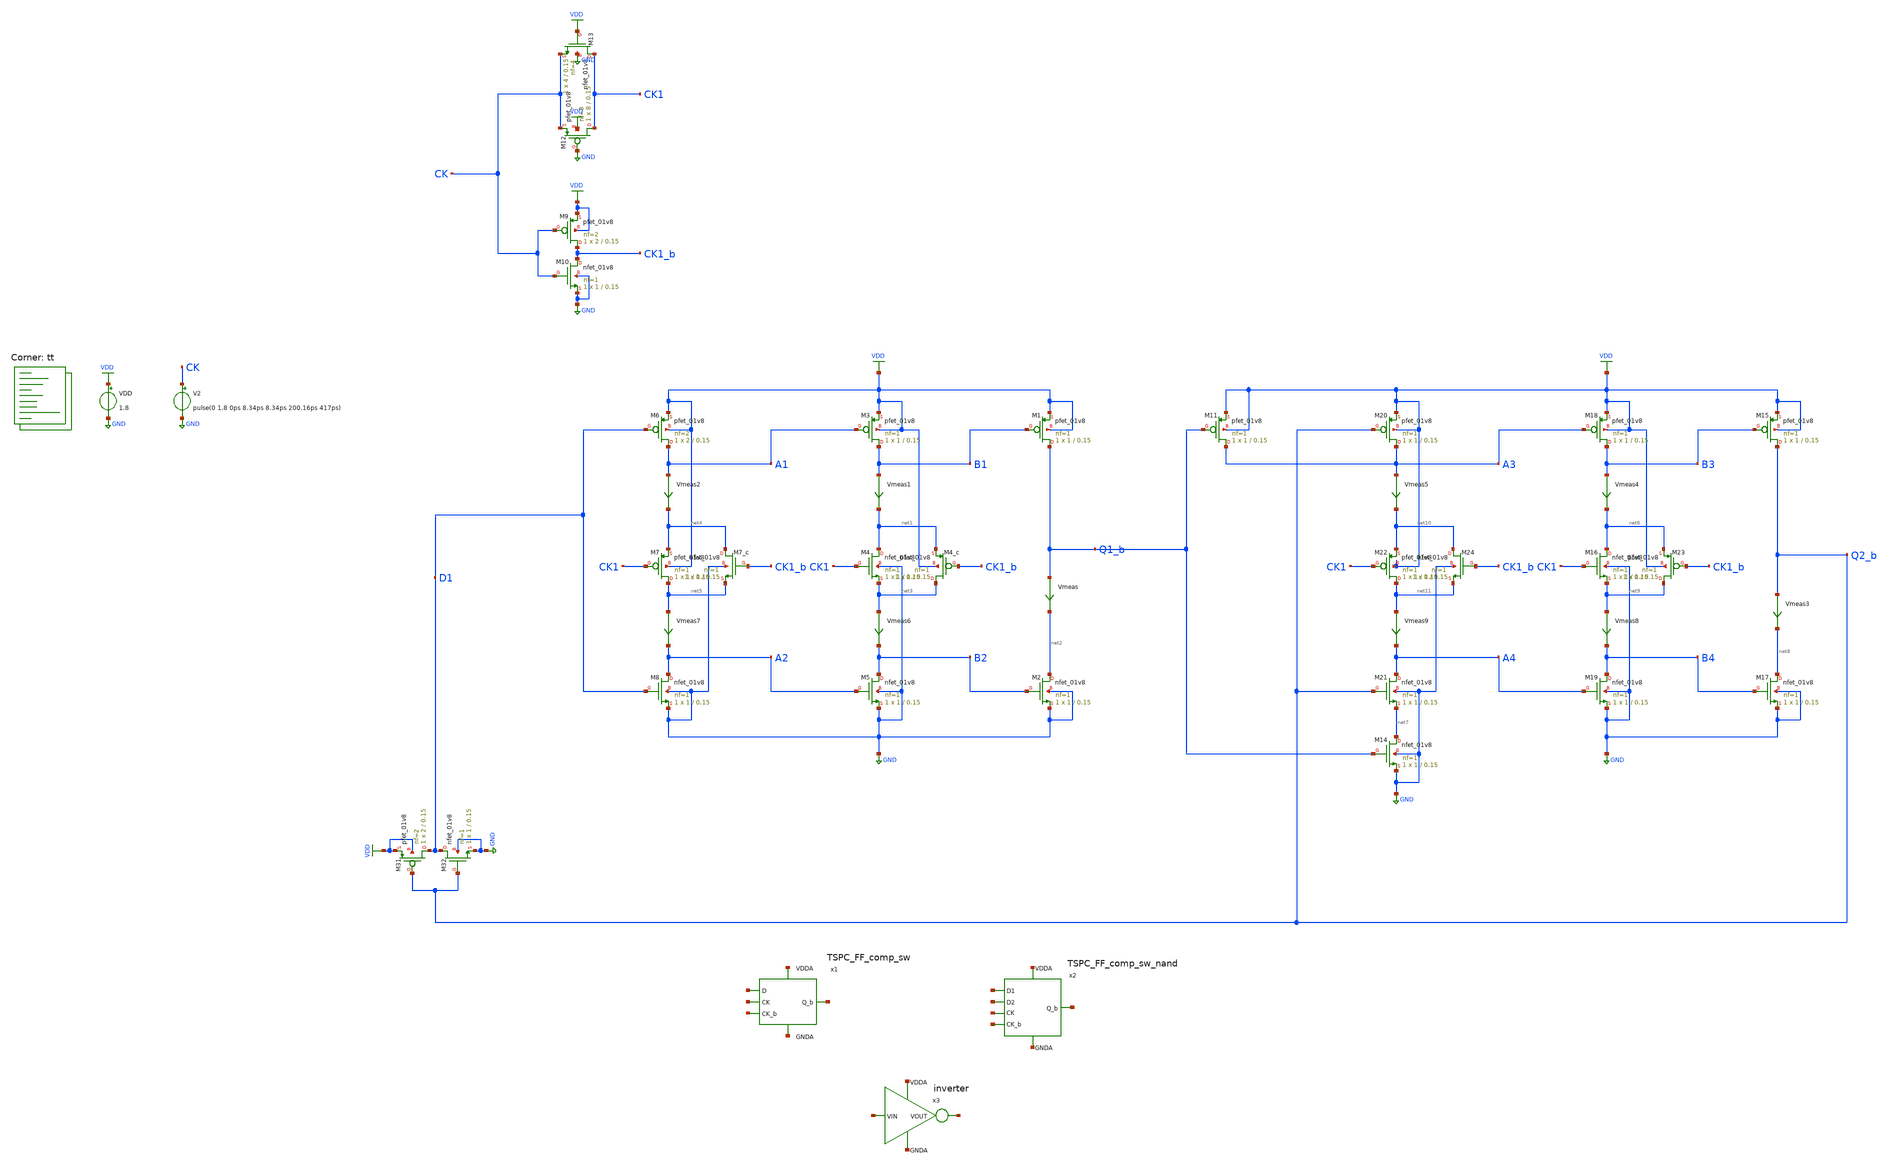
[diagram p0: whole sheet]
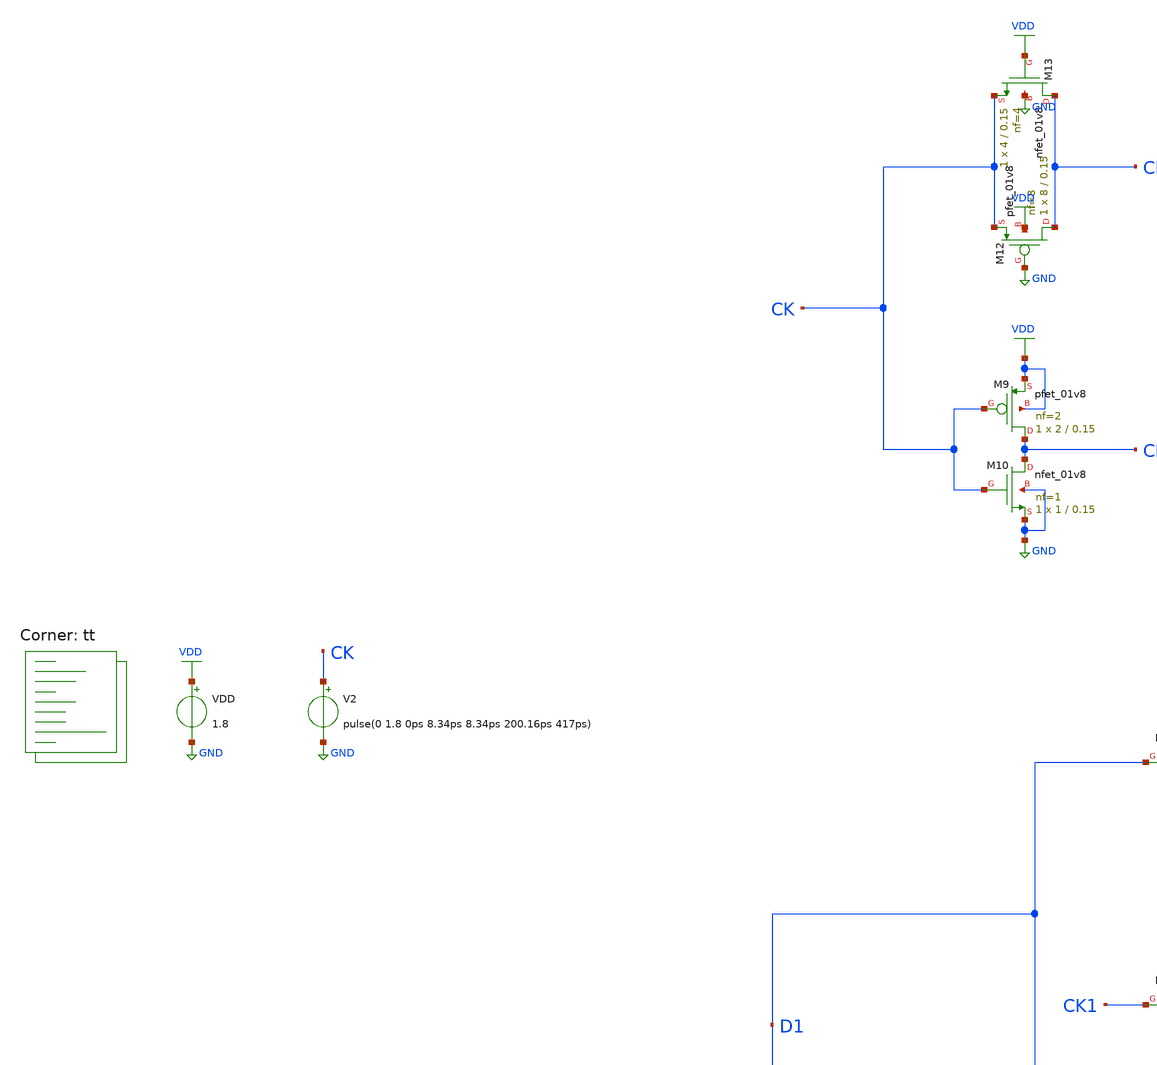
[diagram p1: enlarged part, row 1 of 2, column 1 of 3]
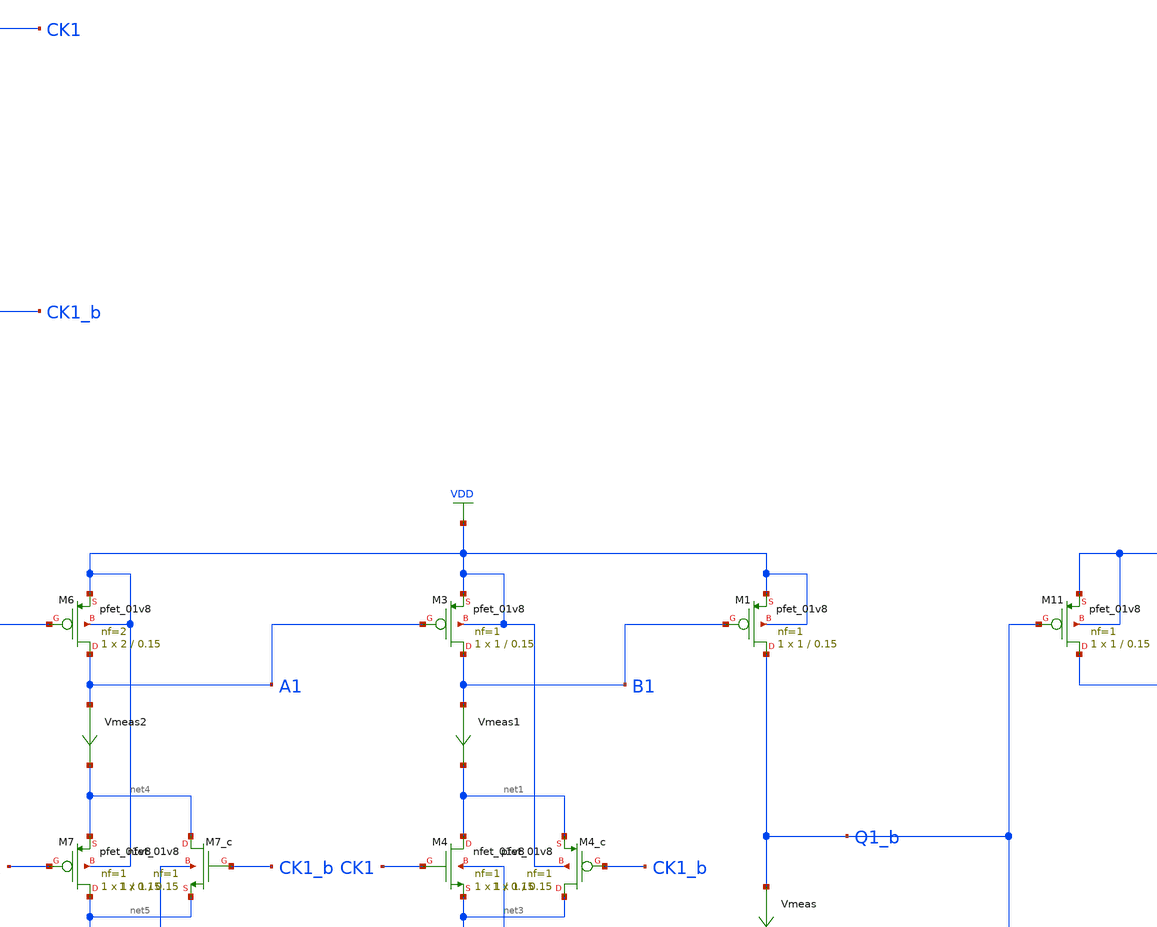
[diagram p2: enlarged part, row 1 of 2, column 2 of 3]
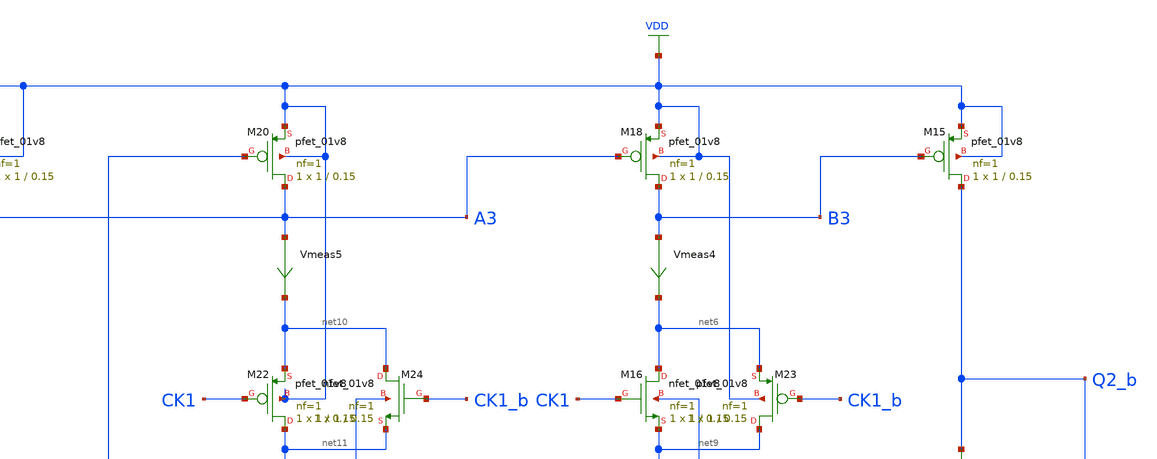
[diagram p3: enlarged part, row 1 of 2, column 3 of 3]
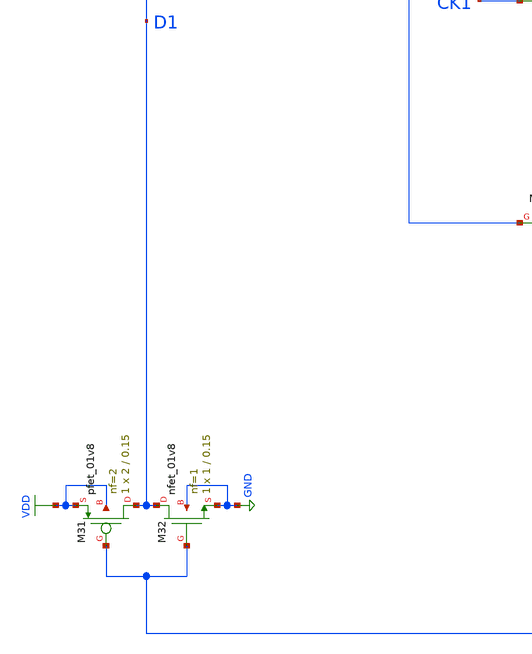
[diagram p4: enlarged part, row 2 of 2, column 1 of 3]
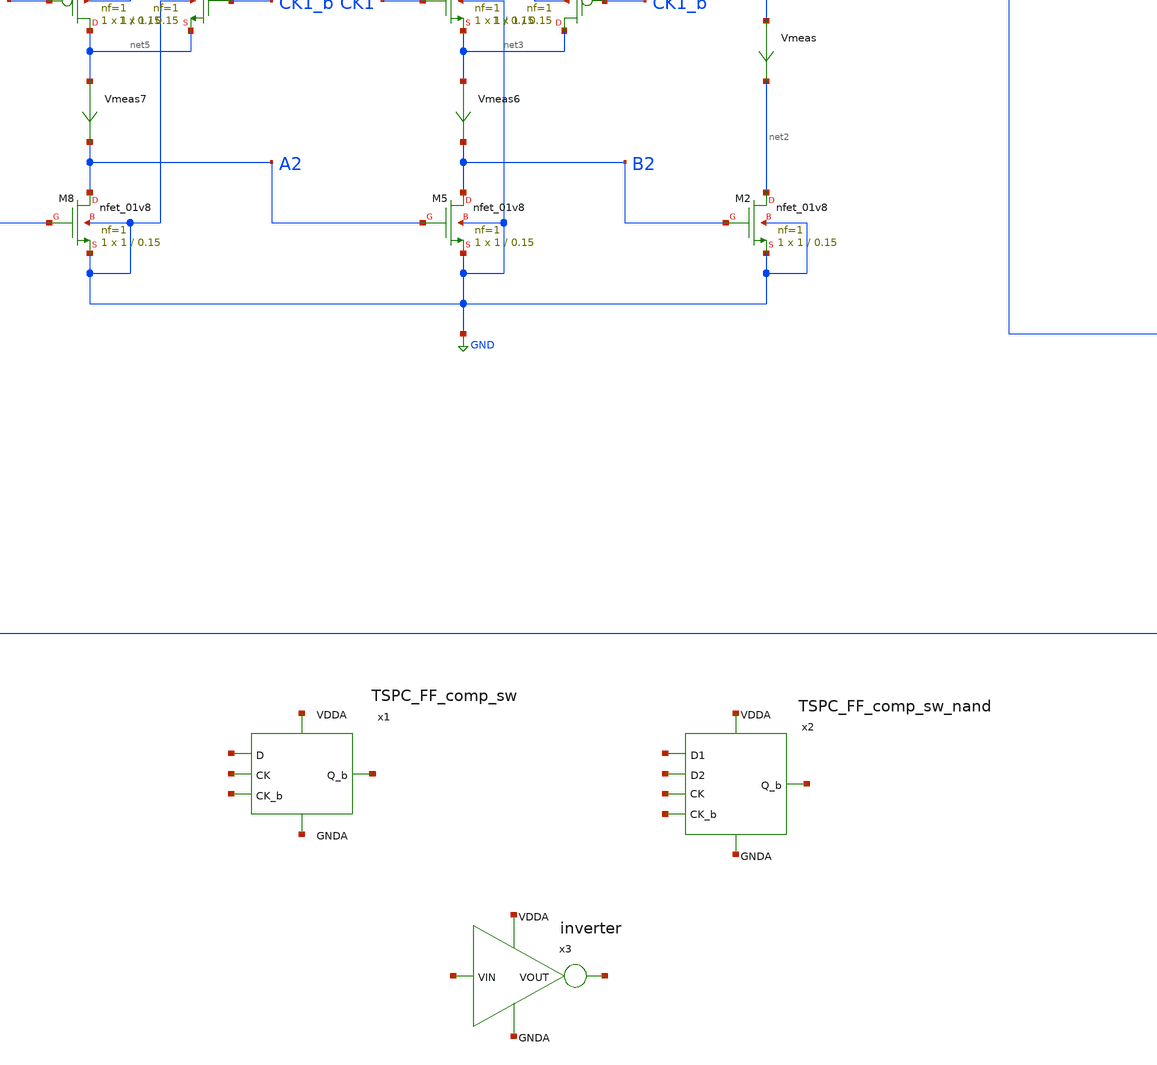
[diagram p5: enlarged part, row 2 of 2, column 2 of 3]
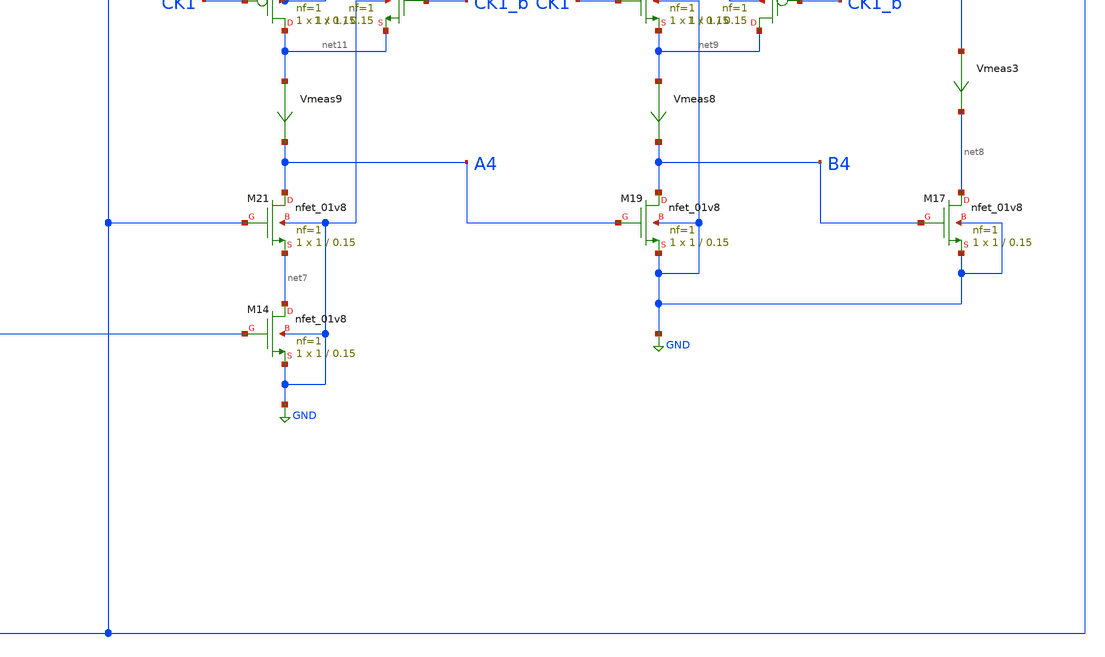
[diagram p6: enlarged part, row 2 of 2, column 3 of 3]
** sch_path: projects/pll/divider/xschem_ngspice/tb_TSPC_FF_comp_sw_divide3_2.sch
**.subckt tb_TSPC_FF_comp_sw_divide3_2
VDD VDD GND 1.8
XM1 Q1_b B1 VDD VDD sky130_fd_pr__pfet_01v8 L=0.15 W=1 nf=1 ad='int((nf+1)/2) * W/nf * 0.29' as='int((nf+2)/2) * W/nf * 0.29'
+ pd='2*int((nf+1)/2) * (W/nf + 0.29)' ps='2*int((nf+2)/2) * (W/nf + 0.29)' nrd='0.29 / W' nrs='0.29 / W'
+ sa=0 sb=0 sd=0 mult=1 m=1
XM4 net1 CK1 net3 GND sky130_fd_pr__nfet_01v8 L=0.15 W=1 nf=1 ad='int((nf+1)/2) * W/nf * 0.29' as='int((nf+2)/2) * W/nf * 0.29'
+ pd='2*int((nf+1)/2) * (W/nf + 0.29)' ps='2*int((nf+2)/2) * (W/nf + 0.29)' nrd='0.29 / W' nrs='0.29 / W'
+ sa=0 sb=0 sd=0 mult=1 m=1
Vmeas Q1_b net2 0
.save i(vmeas)
XM2 net2 B2 GND GND sky130_fd_pr__nfet_01v8 L=0.15 W=1 nf=1 ad='int((nf+1)/2) * W/nf * 0.29' as='int((nf+2)/2) * W/nf * 0.29'
+ pd='2*int((nf+1)/2) * (W/nf + 0.29)' ps='2*int((nf+2)/2) * (W/nf + 0.29)' nrd='0.29 / W' nrs='0.29 / W'
+ sa=0 sb=0 sd=0 mult=1 m=1
XM3 B1 A1 VDD VDD sky130_fd_pr__pfet_01v8 L=0.15 W=1 nf=1 ad='int((nf+1)/2) * W/nf * 0.29' as='int((nf+2)/2) * W/nf * 0.29'
+ pd='2*int((nf+1)/2) * (W/nf + 0.29)' ps='2*int((nf+2)/2) * (W/nf + 0.29)' nrd='0.29 / W' nrs='0.29 / W'
+ sa=0 sb=0 sd=0 mult=1 m=1
XM5 B2 A2 GND GND sky130_fd_pr__nfet_01v8 L=0.15 W=1 nf=1 ad='int((nf+1)/2) * W/nf * 0.29' as='int((nf+2)/2) * W/nf * 0.29'
+ pd='2*int((nf+1)/2) * (W/nf + 0.29)' ps='2*int((nf+2)/2) * (W/nf + 0.29)' nrd='0.29 / W' nrs='0.29 / W'
+ sa=0 sb=0 sd=0 mult=1 m=1
Vmeas1 B1 net1 0
.save i(vmeas1)
XM6 A1 D1 VDD VDD sky130_fd_pr__pfet_01v8 L=0.15 W=2 nf=2 ad='int((nf+1)/2) * W/nf * 0.29' as='int((nf+2)/2) * W/nf * 0.29'
+ pd='2*int((nf+1)/2) * (W/nf + 0.29)' ps='2*int((nf+2)/2) * (W/nf + 0.29)' nrd='0.29 / W' nrs='0.29 / W'
+ sa=0 sb=0 sd=0 mult=1 m=1
XM8 A2 D1 GND GND sky130_fd_pr__nfet_01v8 L=0.15 W=1 nf=1 ad='int((nf+1)/2) * W/nf * 0.29' as='int((nf+2)/2) * W/nf * 0.29'
+ pd='2*int((nf+1)/2) * (W/nf + 0.29)' ps='2*int((nf+2)/2) * (W/nf + 0.29)' nrd='0.29 / W' nrs='0.29 / W'
+ sa=0 sb=0 sd=0 mult=1 m=1
Vmeas2 A1 net4 0
.save i(vmeas2)
XM7 net5 CK1 net4 VDD sky130_fd_pr__pfet_01v8 L=0.15 W=1 nf=1 ad='int((nf+1)/2) * W/nf * 0.29' as='int((nf+2)/2) * W/nf * 0.29'
+ pd='2*int((nf+1)/2) * (W/nf + 0.29)' ps='2*int((nf+2)/2) * (W/nf + 0.29)' nrd='0.29 / W' nrs='0.29 / W'
+ sa=0 sb=0 sd=0 mult=1 m=1
XM4_c net3 CK1_b net1 VDD sky130_fd_pr__pfet_01v8 L=0.15 W=1 nf=1 ad='int((nf+1)/2) * W/nf * 0.29' as='int((nf+2)/2) * W/nf * 0.29'
+ pd='2*int((nf+1)/2) * (W/nf + 0.29)' ps='2*int((nf+2)/2) * (W/nf + 0.29)' nrd='0.29 / W' nrs='0.29 / W'
+ sa=0 sb=0 sd=0 mult=1 m=1
XM7_c net4 CK1_b net5 GND sky130_fd_pr__nfet_01v8 L=0.15 W=1 nf=1 ad='int((nf+1)/2) * W/nf * 0.29' as='int((nf+2)/2) * W/nf * 0.29'
+ pd='2*int((nf+1)/2) * (W/nf + 0.29)' ps='2*int((nf+2)/2) * (W/nf + 0.29)' nrd='0.29 / W' nrs='0.29 / W'
+ sa=0 sb=0 sd=0 mult=1 m=1
XM12 CK1 GND CK VDD sky130_fd_pr__pfet_01v8 L=0.15 W=8 nf=8 ad='int((nf+1)/2) * W/nf * 0.29' as='int((nf+2)/2) * W/nf * 0.29'
+ pd='2*int((nf+1)/2) * (W/nf + 0.29)' ps='2*int((nf+2)/2) * (W/nf + 0.29)' nrd='0.29 / W' nrs='0.29 / W'
+ sa=0 sb=0 sd=0 mult=1 m=1
XM13 CK1 VDD CK GND sky130_fd_pr__nfet_01v8 L=0.15 W=4 nf=4 ad='int((nf+1)/2) * W/nf * 0.29' as='int((nf+2)/2) * W/nf * 0.29'
+ pd='2*int((nf+1)/2) * (W/nf + 0.29)' ps='2*int((nf+2)/2) * (W/nf + 0.29)' nrd='0.29 / W' nrs='0.29 / W'
+ sa=0 sb=0 sd=0 mult=1 m=1
XM9 CK1_b CK VDD VDD sky130_fd_pr__pfet_01v8 L=0.15 W=2 nf=2 ad='int((nf+1)/2) * W/nf * 0.29' as='int((nf+2)/2) * W/nf * 0.29'
+ pd='2*int((nf+1)/2) * (W/nf + 0.29)' ps='2*int((nf+2)/2) * (W/nf + 0.29)' nrd='0.29 / W' nrs='0.29 / W'
+ sa=0 sb=0 sd=0 mult=1 m=1
XM10 CK1_b CK GND GND sky130_fd_pr__nfet_01v8 L=0.15 W=1 nf=1 ad='int((nf+1)/2) * W/nf * 0.29' as='int((nf+2)/2) * W/nf * 0.29'
+ pd='2*int((nf+1)/2) * (W/nf + 0.29)' ps='2*int((nf+2)/2) * (W/nf + 0.29)' nrd='0.29 / W' nrs='0.29 / W'
+ sa=0 sb=0 sd=0 mult=1 m=1
XM15 Q2_b B3 VDD VDD sky130_fd_pr__pfet_01v8 L=0.15 W=1 nf=1 ad='int((nf+1)/2) * W/nf * 0.29' as='int((nf+2)/2) * W/nf * 0.29'
+ pd='2*int((nf+1)/2) * (W/nf + 0.29)' ps='2*int((nf+2)/2) * (W/nf + 0.29)' nrd='0.29 / W' nrs='0.29 / W'
+ sa=0 sb=0 sd=0 mult=1 m=1
XM16 net6 CK1 net9 GND sky130_fd_pr__nfet_01v8 L=0.15 W=1 nf=1 ad='int((nf+1)/2) * W/nf * 0.29' as='int((nf+2)/2) * W/nf * 0.29'
+ pd='2*int((nf+1)/2) * (W/nf + 0.29)' ps='2*int((nf+2)/2) * (W/nf + 0.29)' nrd='0.29 / W' nrs='0.29 / W'
+ sa=0 sb=0 sd=0 mult=1 m=1
Vmeas3 Q2_b net8 0
.save i(vmeas3)
XM17 net8 B4 GND GND sky130_fd_pr__nfet_01v8 L=0.15 W=1 nf=1 ad='int((nf+1)/2) * W/nf * 0.29' as='int((nf+2)/2) * W/nf * 0.29'
+ pd='2*int((nf+1)/2) * (W/nf + 0.29)' ps='2*int((nf+2)/2) * (W/nf + 0.29)' nrd='0.29 / W' nrs='0.29 / W'
+ sa=0 sb=0 sd=0 mult=1 m=1
XM18 B3 A3 VDD VDD sky130_fd_pr__pfet_01v8 L=0.15 W=1 nf=1 ad='int((nf+1)/2) * W/nf * 0.29' as='int((nf+2)/2) * W/nf * 0.29'
+ pd='2*int((nf+1)/2) * (W/nf + 0.29)' ps='2*int((nf+2)/2) * (W/nf + 0.29)' nrd='0.29 / W' nrs='0.29 / W'
+ sa=0 sb=0 sd=0 mult=1 m=1
XM19 B4 A4 GND GND sky130_fd_pr__nfet_01v8 L=0.15 W=1 nf=1 ad='int((nf+1)/2) * W/nf * 0.29' as='int((nf+2)/2) * W/nf * 0.29'
+ pd='2*int((nf+1)/2) * (W/nf + 0.29)' ps='2*int((nf+2)/2) * (W/nf + 0.29)' nrd='0.29 / W' nrs='0.29 / W'
+ sa=0 sb=0 sd=0 mult=1 m=1
Vmeas4 B3 net6 0
.save i(vmeas4)
XM20 A3 Q2_b VDD VDD sky130_fd_pr__pfet_01v8 L=0.15 W=1 nf=1 ad='int((nf+1)/2) * W/nf * 0.29' as='int((nf+2)/2) * W/nf * 0.29'
+ pd='2*int((nf+1)/2) * (W/nf + 0.29)' ps='2*int((nf+2)/2) * (W/nf + 0.29)' nrd='0.29 / W' nrs='0.29 / W'
+ sa=0 sb=0 sd=0 mult=1 m=1
XM21 A4 Q2_b net7 GND sky130_fd_pr__nfet_01v8 L=0.15 W=1 nf=1 ad='int((nf+1)/2) * W/nf * 0.29' as='int((nf+2)/2) * W/nf * 0.29'
+ pd='2*int((nf+1)/2) * (W/nf + 0.29)' ps='2*int((nf+2)/2) * (W/nf + 0.29)' nrd='0.29 / W' nrs='0.29 / W'
+ sa=0 sb=0 sd=0 mult=1 m=1
Vmeas5 A3 net10 0
.save i(vmeas5)
XM22 net11 CK1 net10 VDD sky130_fd_pr__pfet_01v8 L=0.15 W=1 nf=1 ad='int((nf+1)/2) * W/nf * 0.29' as='int((nf+2)/2) * W/nf * 0.29'
+ pd='2*int((nf+1)/2) * (W/nf + 0.29)' ps='2*int((nf+2)/2) * (W/nf + 0.29)' nrd='0.29 / W' nrs='0.29 / W'
+ sa=0 sb=0 sd=0 mult=1 m=1
XM23 net9 CK1_b net6 VDD sky130_fd_pr__pfet_01v8 L=0.15 W=1 nf=1 ad='int((nf+1)/2) * W/nf * 0.29' as='int((nf+2)/2) * W/nf * 0.29'
+ pd='2*int((nf+1)/2) * (W/nf + 0.29)' ps='2*int((nf+2)/2) * (W/nf + 0.29)' nrd='0.29 / W' nrs='0.29 / W'
+ sa=0 sb=0 sd=0 mult=1 m=1
XM24 net10 CK1_b net11 GND sky130_fd_pr__nfet_01v8 L=0.15 W=1 nf=1 ad='int((nf+1)/2) * W/nf * 0.29' as='int((nf+2)/2) * W/nf * 0.29'
+ pd='2*int((nf+1)/2) * (W/nf + 0.29)' ps='2*int((nf+2)/2) * (W/nf + 0.29)' nrd='0.29 / W' nrs='0.29 / W'
+ sa=0 sb=0 sd=0 mult=1 m=1
Vmeas6 net3 B2 0
.save i(vmeas6)
Vmeas7 net5 A2 0
.save i(vmeas7)
Vmeas8 net9 B4 0
.save i(vmeas8)
Vmeas9 net11 A4 0
.save i(vmeas9)
V2 CK GND pulse(0 1.8 0ps 8.34ps 8.34ps 200.16ps 417ps)
XM31 D1 Q2_b VDD VDD sky130_fd_pr__pfet_01v8 L=0.15 W=2 nf=2 ad='int((nf+1)/2) * W/nf * 0.29' as='int((nf+2)/2) * W/nf * 0.29'
+ pd='2*int((nf+1)/2) * (W/nf + 0.29)' ps='2*int((nf+2)/2) * (W/nf + 0.29)' nrd='0.29 / W' nrs='0.29 / W'
+ sa=0 sb=0 sd=0 mult=1 m=1
XM32 D1 Q2_b GND GND sky130_fd_pr__nfet_01v8 L=0.15 W=1 nf=1 ad='int((nf+1)/2) * W/nf * 0.29' as='int((nf+2)/2) * W/nf * 0.29'
+ pd='2*int((nf+1)/2) * (W/nf + 0.29)' ps='2*int((nf+2)/2) * (W/nf + 0.29)' nrd='0.29 / W' nrs='0.29 / W'
+ sa=0 sb=0 sd=0 mult=1 m=1
XM11 A3 Q1_b VDD VDD sky130_fd_pr__pfet_01v8 L=0.15 W=1 nf=1 ad='int((nf+1)/2) * W/nf * 0.29' as='int((nf+2)/2) * W/nf * 0.29'
+ pd='2*int((nf+1)/2) * (W/nf + 0.29)' ps='2*int((nf+2)/2) * (W/nf + 0.29)' nrd='0.29 / W' nrs='0.29 / W'
+ sa=0 sb=0 sd=0 mult=1 m=1
XM14 net7 Q1_b GND GND sky130_fd_pr__nfet_01v8 L=0.15 W=1 nf=1 ad='int((nf+1)/2) * W/nf * 0.29' as='int((nf+2)/2) * W/nf * 0.29'
+ pd='2*int((nf+1)/2) * (W/nf + 0.29)' ps='2*int((nf+2)/2) * (W/nf + 0.29)' nrd='0.29 / W' nrs='0.29 / W'
+ sa=0 sb=0 sd=0 mult=1 m=1
x1 net12 net13 net14 net15 net16 net17 TSPC_FF_comp_sw
x2 net18 net19 net20 net21 net22 net23 net24 TSPC_FF_comp_sw_nand
x3 net25 net26 net27 net28 inverter
**** begin user architecture code



.include /foss/pdks/sky130A/libs.ref/sky130_fd_sc_hd/spice/sky130_fd_sc_hd.spice

.option method=gear
.option wnflag=1
.option savecurrents

.save @m.xm1.msky130_fd_pr__pfet_01v8[gm] @m.xm2.msky130_fd_pr__nfet_01v8[gm] @m.xm3.msky130_fd_pr__pfet_01v8[gm] @m.xm4.msky130_fd_pr__nfet_01v8[gm] @m.xm4_c.msky130_fd_pr__pfet_01v8[gm] @m.xm5.msky130_fd_pr__nfet_01v8[gm] @m.xm6.msky130_fd_pr__pfet_01v8[gm] @m.xm7.msky130_fd_pr__pfet_01v8[gm] @m.xm7_c.msky130_fd_pr__nfet_01v8[gm] @m.xm8.msky130_fd_pr__nfet_01v8[gm]

*.ic v(d)=0
*.ic v(q)=0
*.ic v(q1)=0

.control

  save v(d1) v(d2) v(q1) v(q2) v(q1_b) v(q2_b) v(q3) v(a1) v(a2) v(a3) v(a4) v(b1) v(b2) v(b3) v(b4)
+ v(ck) v(ck1) v(ck1_b)
  * save all
  * tran 0.1n 1u
  tran 1p 20n

  remzerovec
  write tb_TSPC_FF_comp_sw_divide3_2.raw
  * set appendwrite

.endc



.lib $::SKYWATER_MODELS/sky130.lib.spice tt
**** end user architecture code
**.ends

* expanding   symbol:
*+  /foss/designs/my_design/projects/pll/divider/xschem_ngspice/TSPC_FF_comp_sw.sym # of pins=6
** sym_path: projects/pll/divider/xschem_ngspice/TSPC_FF_comp_sw.sym
** sch_path: projects/pll/divider/xschem_ngspice/TSPC_FF_comp_sw.sch
.subckt TSPC_FF_comp_sw VDDA Q_b D CK_b GNDA CK
*.ipin CK
*.ipin D
*.opin Q_b
*.ipin VDDA
*.ipin GNDA
*.ipin CK_b
XM1 Q_b net1 VDDA VDDA sky130_fd_pr__pfet_01v8 L=0.15 W=1 nf=1 ad='int((nf+1)/2) * W/nf * 0.29' as='int((nf+2)/2) * W/nf * 0.29'
+ pd='2*int((nf+1)/2) * (W/nf + 0.29)' ps='2*int((nf+2)/2) * (W/nf + 0.29)' nrd='0.29 / W' nrs='0.29 / W'
+ sa=0 sb=0 sd=0 mult=1 m=1
XM4 net1 CK net2 GNDA sky130_fd_pr__nfet_01v8 L=0.15 W=1 nf=1 ad='int((nf+1)/2) * W/nf * 0.29' as='int((nf+2)/2) * W/nf * 0.29'
+ pd='2*int((nf+1)/2) * (W/nf + 0.29)' ps='2*int((nf+2)/2) * (W/nf + 0.29)' nrd='0.29 / W' nrs='0.29 / W'
+ sa=0 sb=0 sd=0 mult=1 m=1
XM2 Q_b net2 GNDA GNDA sky130_fd_pr__nfet_01v8 L=0.15 W=1 nf=1 ad='int((nf+1)/2) * W/nf * 0.29' as='int((nf+2)/2) * W/nf * 0.29'
+ pd='2*int((nf+1)/2) * (W/nf + 0.29)' ps='2*int((nf+2)/2) * (W/nf + 0.29)' nrd='0.29 / W' nrs='0.29 / W'
+ sa=0 sb=0 sd=0 mult=1 m=1
XM3 net1 net4 VDDA VDDA sky130_fd_pr__pfet_01v8 L=0.15 W=1 nf=1 ad='int((nf+1)/2) * W/nf * 0.29' as='int((nf+2)/2) * W/nf * 0.29'
+ pd='2*int((nf+1)/2) * (W/nf + 0.29)' ps='2*int((nf+2)/2) * (W/nf + 0.29)' nrd='0.29 / W' nrs='0.29 / W'
+ sa=0 sb=0 sd=0 mult=1 m=1
XM5 net2 net3 GNDA GNDA sky130_fd_pr__nfet_01v8 L=0.15 W=1 nf=1 ad='int((nf+1)/2) * W/nf * 0.29' as='int((nf+2)/2) * W/nf * 0.29'
+ pd='2*int((nf+1)/2) * (W/nf + 0.29)' ps='2*int((nf+2)/2) * (W/nf + 0.29)' nrd='0.29 / W' nrs='0.29 / W'
+ sa=0 sb=0 sd=0 mult=1 m=1
XM6 net4 D VDDA VDDA sky130_fd_pr__pfet_01v8 L=0.15 W=1 nf=1 ad='int((nf+1)/2) * W/nf * 0.29' as='int((nf+2)/2) * W/nf * 0.29'
+ pd='2*int((nf+1)/2) * (W/nf + 0.29)' ps='2*int((nf+2)/2) * (W/nf + 0.29)' nrd='0.29 / W' nrs='0.29 / W'
+ sa=0 sb=0 sd=0 mult=1 m=1
XM8 net3 D GNDA GNDA sky130_fd_pr__nfet_01v8 L=0.15 W=1 nf=1 ad='int((nf+1)/2) * W/nf * 0.29' as='int((nf+2)/2) * W/nf * 0.29'
+ pd='2*int((nf+1)/2) * (W/nf + 0.29)' ps='2*int((nf+2)/2) * (W/nf + 0.29)' nrd='0.29 / W' nrs='0.29 / W'
+ sa=0 sb=0 sd=0 mult=1 m=1
XM7 net3 CK net4 VDDA sky130_fd_pr__pfet_01v8 L=0.15 W=1 nf=1 ad='int((nf+1)/2) * W/nf * 0.29' as='int((nf+2)/2) * W/nf * 0.29'
+ pd='2*int((nf+1)/2) * (W/nf + 0.29)' ps='2*int((nf+2)/2) * (W/nf + 0.29)' nrd='0.29 / W' nrs='0.29 / W'
+ sa=0 sb=0 sd=0 mult=1 m=1
XM4_c net2 CK_b net1 VDDA sky130_fd_pr__pfet_01v8 L=0.15 W=1 nf=1 ad='int((nf+1)/2) * W/nf * 0.29' as='int((nf+2)/2) * W/nf * 0.29'
+ pd='2*int((nf+1)/2) * (W/nf + 0.29)' ps='2*int((nf+2)/2) * (W/nf + 0.29)' nrd='0.29 / W' nrs='0.29 / W'
+ sa=0 sb=0 sd=0 mult=1 m=1
XM7_c net4 CK_b net3 GNDA sky130_fd_pr__nfet_01v8 L=0.15 W=1 nf=1 ad='int((nf+1)/2) * W/nf * 0.29' as='int((nf+2)/2) * W/nf * 0.29'
+ pd='2*int((nf+1)/2) * (W/nf + 0.29)' ps='2*int((nf+2)/2) * (W/nf + 0.29)' nrd='0.29 / W' nrs='0.29 / W'
+ sa=0 sb=0 sd=0 mult=1 m=1
.ends


* expanding   symbol:
*+  /foss/designs/my_design/projects/pll/divider/xschem_ngspice/TSPC_FF_comp_sw_nand.sym # of pins=7
** sym_path: projects/pll/divider/xschem_ngspice/TSPC_FF_comp_sw_nand.sym
** sch_path: projects/pll/divider/xschem_ngspice/TSPC_FF_comp_sw_nand.sch
.subckt TSPC_FF_comp_sw_nand VDDA Q_b D2 D1 CK_b CK GNDA
*.ipin CK
*.ipin D1
*.opin Q_b
*.ipin VDDA
*.ipin GNDA
*.ipin CK_b
*.ipin D2
XM1 Q_b net2 VDDA VDDA sky130_fd_pr__pfet_01v8 L=0.15 W=1 nf=1 ad='int((nf+1)/2) * W/nf * 0.29' as='int((nf+2)/2) * W/nf * 0.29'
+ pd='2*int((nf+1)/2) * (W/nf + 0.29)' ps='2*int((nf+2)/2) * (W/nf + 0.29)' nrd='0.29 / W' nrs='0.29 / W'
+ sa=0 sb=0 sd=0 mult=1 m=1
XM4 net2 CK net1 GNDA sky130_fd_pr__nfet_01v8 L=0.15 W=1 nf=1 ad='int((nf+1)/2) * W/nf * 0.29' as='int((nf+2)/2) * W/nf * 0.29'
+ pd='2*int((nf+1)/2) * (W/nf + 0.29)' ps='2*int((nf+2)/2) * (W/nf + 0.29)' nrd='0.29 / W' nrs='0.29 / W'
+ sa=0 sb=0 sd=0 mult=1 m=1
XM2 Q_b net1 GNDA GNDA sky130_fd_pr__nfet_01v8 L=0.15 W=1 nf=1 ad='int((nf+1)/2) * W/nf * 0.29' as='int((nf+2)/2) * W/nf * 0.29'
+ pd='2*int((nf+1)/2) * (W/nf + 0.29)' ps='2*int((nf+2)/2) * (W/nf + 0.29)' nrd='0.29 / W' nrs='0.29 / W'
+ sa=0 sb=0 sd=0 mult=1 m=1
XM3 net2 net4 VDDA VDDA sky130_fd_pr__pfet_01v8 L=0.15 W=1 nf=1 ad='int((nf+1)/2) * W/nf * 0.29' as='int((nf+2)/2) * W/nf * 0.29'
+ pd='2*int((nf+1)/2) * (W/nf + 0.29)' ps='2*int((nf+2)/2) * (W/nf + 0.29)' nrd='0.29 / W' nrs='0.29 / W'
+ sa=0 sb=0 sd=0 mult=1 m=1
XM5 net1 net3 GNDA GNDA sky130_fd_pr__nfet_01v8 L=0.15 W=1 nf=1 ad='int((nf+1)/2) * W/nf * 0.29' as='int((nf+2)/2) * W/nf * 0.29'
+ pd='2*int((nf+1)/2) * (W/nf + 0.29)' ps='2*int((nf+2)/2) * (W/nf + 0.29)' nrd='0.29 / W' nrs='0.29 / W'
+ sa=0 sb=0 sd=0 mult=1 m=1
XM6 net4 D2 VDDA VDDA sky130_fd_pr__pfet_01v8 L=0.15 W=1 nf=1 ad='int((nf+1)/2) * W/nf * 0.29' as='int((nf+2)/2) * W/nf * 0.29'
+ pd='2*int((nf+1)/2) * (W/nf + 0.29)' ps='2*int((nf+2)/2) * (W/nf + 0.29)' nrd='0.29 / W' nrs='0.29 / W'
+ sa=0 sb=0 sd=0 mult=1 m=1
XM10 net5 D1 GNDA GNDA sky130_fd_pr__nfet_01v8 L=0.15 W=1 nf=1 ad='int((nf+1)/2) * W/nf * 0.29' as='int((nf+2)/2) * W/nf * 0.29'
+ pd='2*int((nf+1)/2) * (W/nf + 0.29)' ps='2*int((nf+2)/2) * (W/nf + 0.29)' nrd='0.29 / W' nrs='0.29 / W'
+ sa=0 sb=0 sd=0 mult=1 m=1
XM8 net3 CK net4 VDDA sky130_fd_pr__pfet_01v8 L=0.15 W=1 nf=1 ad='int((nf+1)/2) * W/nf * 0.29' as='int((nf+2)/2) * W/nf * 0.29'
+ pd='2*int((nf+1)/2) * (W/nf + 0.29)' ps='2*int((nf+2)/2) * (W/nf + 0.29)' nrd='0.29 / W' nrs='0.29 / W'
+ sa=0 sb=0 sd=0 mult=1 m=1
XM4_c net1 CK_b net2 VDDA sky130_fd_pr__pfet_01v8 L=0.15 W=1 nf=1 ad='int((nf+1)/2) * W/nf * 0.29' as='int((nf+2)/2) * W/nf * 0.29'
+ pd='2*int((nf+1)/2) * (W/nf + 0.29)' ps='2*int((nf+2)/2) * (W/nf + 0.29)' nrd='0.29 / W' nrs='0.29 / W'
+ sa=0 sb=0 sd=0 mult=1 m=1
XM8_c net4 CK_b net3 GNDA sky130_fd_pr__nfet_01v8 L=0.15 W=1 nf=1 ad='int((nf+1)/2) * W/nf * 0.29' as='int((nf+2)/2) * W/nf * 0.29'
+ pd='2*int((nf+1)/2) * (W/nf + 0.29)' ps='2*int((nf+2)/2) * (W/nf + 0.29)' nrd='0.29 / W' nrs='0.29 / W'
+ sa=0 sb=0 sd=0 mult=1 m=1
XM9 net3 D2 net5 GNDA sky130_fd_pr__nfet_01v8 L=0.15 W=1 nf=1 ad='int((nf+1)/2) * W/nf * 0.29' as='int((nf+2)/2) * W/nf * 0.29'
+ pd='2*int((nf+1)/2) * (W/nf + 0.29)' ps='2*int((nf+2)/2) * (W/nf + 0.29)' nrd='0.29 / W' nrs='0.29 / W'
+ sa=0 sb=0 sd=0 mult=1 m=1
XM7 net4 D1 VDDA VDDA sky130_fd_pr__pfet_01v8 L=0.15 W=1 nf=1 ad='int((nf+1)/2) * W/nf * 0.29' as='int((nf+2)/2) * W/nf * 0.29'
+ pd='2*int((nf+1)/2) * (W/nf + 0.29)' ps='2*int((nf+2)/2) * (W/nf + 0.29)' nrd='0.29 / W' nrs='0.29 / W'
+ sa=0 sb=0 sd=0 mult=1 m=1
.ends


* expanding   symbol:  /foss/designs/my_design/projects/pll/divider/xschem_ngspice/inverter.sym # of
*+ pins=4
** sym_path: projects/pll/divider/xschem_ngspice/inverter.sym
** sch_path: projects/pll/divider/xschem_ngspice/inverter.sch
.subckt inverter VDDA VIN VOUT GNDA
*.ipin VIN
*.ipin VDDA
*.ipin GNDA
*.opin VOUT
XM31 VOUT VIN VDDA VDDA sky130_fd_pr__pfet_01v8 L=0.15 W=2 nf=2 ad='int((nf+1)/2) * W/nf * 0.29' as='int((nf+2)/2) * W/nf * 0.29'
+ pd='2*int((nf+1)/2) * (W/nf + 0.29)' ps='2*int((nf+2)/2) * (W/nf + 0.29)' nrd='0.29 / W' nrs='0.29 / W'
+ sa=0 sb=0 sd=0 mult=1 m=1
XM32 VOUT VIN GNDA GNDA sky130_fd_pr__nfet_01v8 L=0.15 W=1 nf=1 ad='int((nf+1)/2) * W/nf * 0.29' as='int((nf+2)/2) * W/nf * 0.29'
+ pd='2*int((nf+1)/2) * (W/nf + 0.29)' ps='2*int((nf+2)/2) * (W/nf + 0.29)' nrd='0.29 / W' nrs='0.29 / W'
+ sa=0 sb=0 sd=0 mult=1 m=1
.ends

.GLOBAL GND
.GLOBAL VDD
.end
